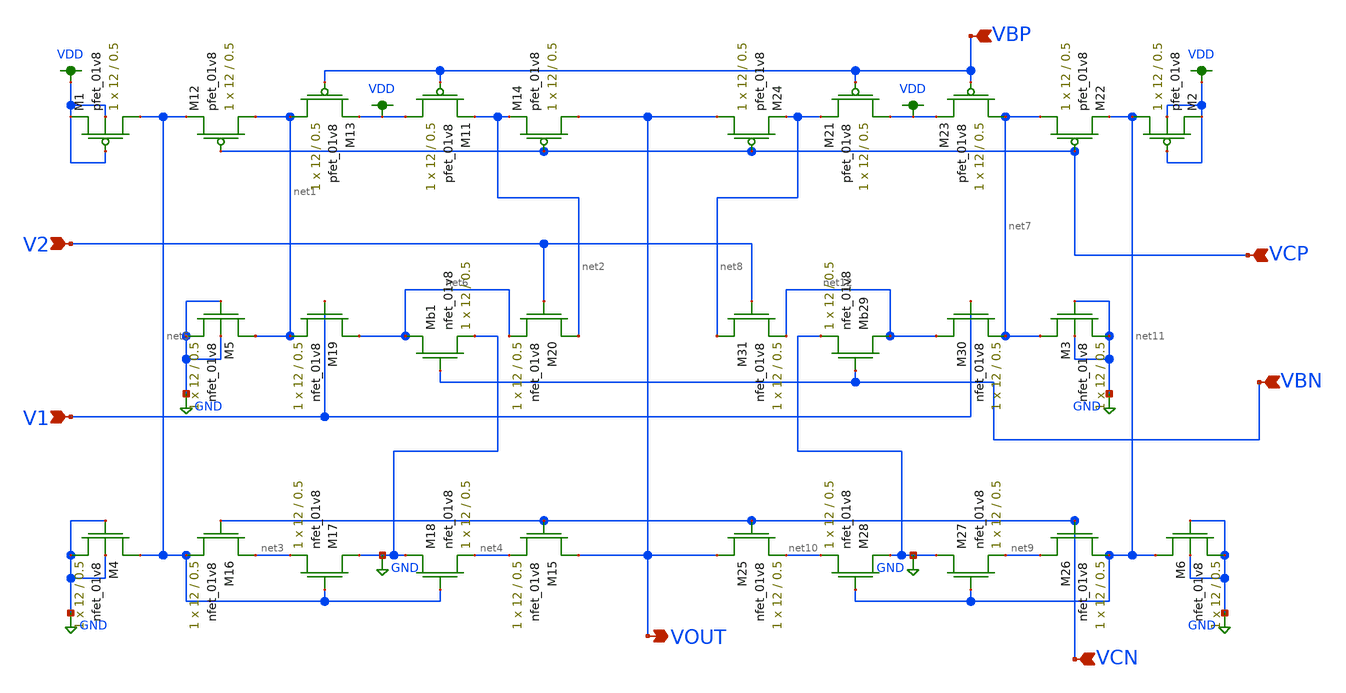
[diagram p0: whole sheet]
** sch_path: MP3/LDS_FCDA.sch
**.subckt LDS_FCDA VBP VCN VCP VOUT VBN V2 V1
*.ipin VBP
*.ipin VCN
*.ipin VCP
*.opin VOUT
*.ipin VBN
*.ipin V2
*.ipin V1
XM11 VDD VBP net2 VDD sky130_fd_pr__pfet_01v8 L=0.5 W=12 nf=1 ad='int((nf+1)/2) * W/nf * 0.29' as='int((nf+2)/2) * W/nf * 0.29'
+ pd='2*int((nf+1)/2) * (W/nf + 0.29)' ps='2*int((nf+2)/2) * (W/nf + 0.29)' nrd='0.29 / W' nrs='0.29 / W'
+ sa=0 sb=0 sd=0 mult=1 m=1
XM12 net1 VCP net5 VDD sky130_fd_pr__pfet_01v8 L=0.5 W=12 nf=1 ad='int((nf+1)/2) * W/nf * 0.29' as='int((nf+2)/2) * W/nf * 0.29'
+ pd='2*int((nf+1)/2) * (W/nf + 0.29)' ps='2*int((nf+2)/2) * (W/nf + 0.29)' nrd='0.29 / W' nrs='0.29 / W'
+ sa=0 sb=0 sd=0 mult=1 m=1
XM13 net1 VBP VDD VDD sky130_fd_pr__pfet_01v8 L=0.5 W=12 nf=1 ad='int((nf+1)/2) * W/nf * 0.29' as='int((nf+2)/2) * W/nf * 0.29'
+ pd='2*int((nf+1)/2) * (W/nf + 0.29)' ps='2*int((nf+2)/2) * (W/nf + 0.29)' nrd='0.29 / W' nrs='0.29 / W'
+ sa=0 sb=0 sd=0 mult=1 m=1
XM14 VOUT VCP net2 VDD sky130_fd_pr__pfet_01v8 L=0.5 W=12 nf=1 ad='int((nf+1)/2) * W/nf * 0.29' as='int((nf+2)/2) * W/nf * 0.29'
+ pd='2*int((nf+1)/2) * (W/nf + 0.29)' ps='2*int((nf+2)/2) * (W/nf + 0.29)' nrd='0.29 / W' nrs='0.29 / W'
+ sa=0 sb=0 sd=0 mult=1 m=1
XM15 VOUT VCN net4 GND sky130_fd_pr__nfet_01v8 L=0.5 W=12 nf=1 ad='int((nf+1)/2) * W/nf * 0.29' as='int((nf+2)/2) * W/nf * 0.29'
+ pd='2*int((nf+1)/2) * (W/nf + 0.29)' ps='2*int((nf+2)/2) * (W/nf + 0.29)' nrd='0.29 / W' nrs='0.29 / W'
+ sa=0 sb=0 sd=0 mult=1 m=1
XM16 net3 VCN net5 GND sky130_fd_pr__nfet_01v8 L=0.5 W=12 nf=1 ad='int((nf+1)/2) * W/nf * 0.29' as='int((nf+2)/2) * W/nf * 0.29'
+ pd='2*int((nf+1)/2) * (W/nf + 0.29)' ps='2*int((nf+2)/2) * (W/nf + 0.29)' nrd='0.29 / W' nrs='0.29 / W'
+ sa=0 sb=0 sd=0 mult=1 m=1
XM17 GND net5 net3 GND sky130_fd_pr__nfet_01v8 L=0.5 W=12 nf=1 ad='int((nf+1)/2) * W/nf * 0.29' as='int((nf+2)/2) * W/nf * 0.29'
+ pd='2*int((nf+1)/2) * (W/nf + 0.29)' ps='2*int((nf+2)/2) * (W/nf + 0.29)' nrd='0.29 / W' nrs='0.29 / W'
+ sa=0 sb=0 sd=0 mult=1 m=1
XM18 GND net5 net4 GND sky130_fd_pr__nfet_01v8 L=0.5 W=12 nf=1 ad='int((nf+1)/2) * W/nf * 0.29' as='int((nf+2)/2) * W/nf * 0.29'
+ pd='2*int((nf+1)/2) * (W/nf + 0.29)' ps='2*int((nf+2)/2) * (W/nf + 0.29)' nrd='0.29 / W' nrs='0.29 / W'
+ sa=0 sb=0 sd=0 mult=1 m=1
XMb1 net6 VBN GND GND sky130_fd_pr__nfet_01v8 L=0.5 W=12 nf=1 ad='int((nf+1)/2) * W/nf * 0.29' as='int((nf+2)/2) * W/nf * 0.29'
+ pd='2*int((nf+1)/2) * (W/nf + 0.29)' ps='2*int((nf+2)/2) * (W/nf + 0.29)' nrd='0.29 / W' nrs='0.29 / W'
+ sa=0 sb=0 sd=0 mult=1 m=1
XM19 net6 V1 net1 GND sky130_fd_pr__nfet_01v8 L=0.5 W=12 nf=1 ad='int((nf+1)/2) * W/nf * 0.29' as='int((nf+2)/2) * W/nf * 0.29'
+ pd='2*int((nf+1)/2) * (W/nf + 0.29)' ps='2*int((nf+2)/2) * (W/nf + 0.29)' nrd='0.29 / W' nrs='0.29 / W'
+ sa=0 sb=0 sd=0 mult=1 m=1
XM20 net2 V2 net6 GND sky130_fd_pr__nfet_01v8 L=0.5 W=12 nf=1 ad='int((nf+1)/2) * W/nf * 0.29' as='int((nf+2)/2) * W/nf * 0.29'
+ pd='2*int((nf+1)/2) * (W/nf + 0.29)' ps='2*int((nf+2)/2) * (W/nf + 0.29)' nrd='0.29 / W' nrs='0.29 / W'
+ sa=0 sb=0 sd=0 mult=1 m=1
XM21 VDD VBP net8 VDD sky130_fd_pr__pfet_01v8 L=0.5 W=12 nf=1 ad='int((nf+1)/2) * W/nf * 0.29' as='int((nf+2)/2) * W/nf * 0.29'
+ pd='2*int((nf+1)/2) * (W/nf + 0.29)' ps='2*int((nf+2)/2) * (W/nf + 0.29)' nrd='0.29 / W' nrs='0.29 / W'
+ sa=0 sb=0 sd=0 mult=1 m=1
XM22 net7 VCP net11 VDD sky130_fd_pr__pfet_01v8 L=0.5 W=12 nf=1 ad='int((nf+1)/2) * W/nf * 0.29' as='int((nf+2)/2) * W/nf * 0.29'
+ pd='2*int((nf+1)/2) * (W/nf + 0.29)' ps='2*int((nf+2)/2) * (W/nf + 0.29)' nrd='0.29 / W' nrs='0.29 / W'
+ sa=0 sb=0 sd=0 mult=1 m=1
XM23 net7 VBP VDD VDD sky130_fd_pr__pfet_01v8 L=0.5 W=12 nf=1 ad='int((nf+1)/2) * W/nf * 0.29' as='int((nf+2)/2) * W/nf * 0.29'
+ pd='2*int((nf+1)/2) * (W/nf + 0.29)' ps='2*int((nf+2)/2) * (W/nf + 0.29)' nrd='0.29 / W' nrs='0.29 / W'
+ sa=0 sb=0 sd=0 mult=1 m=1
XM24 VOUT VCP net8 VDD sky130_fd_pr__pfet_01v8 L=0.5 W=12 nf=1 ad='int((nf+1)/2) * W/nf * 0.29' as='int((nf+2)/2) * W/nf * 0.29'
+ pd='2*int((nf+1)/2) * (W/nf + 0.29)' ps='2*int((nf+2)/2) * (W/nf + 0.29)' nrd='0.29 / W' nrs='0.29 / W'
+ sa=0 sb=0 sd=0 mult=1 m=1
XM25 VOUT VCN net10 GND sky130_fd_pr__nfet_01v8 L=0.5 W=12 nf=1 ad='int((nf+1)/2) * W/nf * 0.29' as='int((nf+2)/2) * W/nf * 0.29'
+ pd='2*int((nf+1)/2) * (W/nf + 0.29)' ps='2*int((nf+2)/2) * (W/nf + 0.29)' nrd='0.29 / W' nrs='0.29 / W'
+ sa=0 sb=0 sd=0 mult=1 m=1
XM26 net9 VCN net11 GND sky130_fd_pr__nfet_01v8 L=0.5 W=12 nf=1 ad='int((nf+1)/2) * W/nf * 0.29' as='int((nf+2)/2) * W/nf * 0.29'
+ pd='2*int((nf+1)/2) * (W/nf + 0.29)' ps='2*int((nf+2)/2) * (W/nf + 0.29)' nrd='0.29 / W' nrs='0.29 / W'
+ sa=0 sb=0 sd=0 mult=1 m=1
XM27 GND net11 net9 GND sky130_fd_pr__nfet_01v8 L=0.5 W=12 nf=1 ad='int((nf+1)/2) * W/nf * 0.29' as='int((nf+2)/2) * W/nf * 0.29'
+ pd='2*int((nf+1)/2) * (W/nf + 0.29)' ps='2*int((nf+2)/2) * (W/nf + 0.29)' nrd='0.29 / W' nrs='0.29 / W'
+ sa=0 sb=0 sd=0 mult=1 m=1
XM28 GND net11 net10 GND sky130_fd_pr__nfet_01v8 L=0.5 W=12 nf=1 ad='int((nf+1)/2) * W/nf * 0.29' as='int((nf+2)/2) * W/nf * 0.29'
+ pd='2*int((nf+1)/2) * (W/nf + 0.29)' ps='2*int((nf+2)/2) * (W/nf + 0.29)' nrd='0.29 / W' nrs='0.29 / W'
+ sa=0 sb=0 sd=0 mult=1 m=1
XMb29 net12 VBN GND GND sky130_fd_pr__nfet_01v8 L=0.5 W=12 nf=1 ad='int((nf+1)/2) * W/nf * 0.29' as='int((nf+2)/2) * W/nf * 0.29'
+ pd='2*int((nf+1)/2) * (W/nf + 0.29)' ps='2*int((nf+2)/2) * (W/nf + 0.29)' nrd='0.29 / W' nrs='0.29 / W'
+ sa=0 sb=0 sd=0 mult=1 m=1
XM30 net12 V1 net7 GND sky130_fd_pr__nfet_01v8 L=0.5 W=12 nf=1 ad='int((nf+1)/2) * W/nf * 0.29' as='int((nf+2)/2) * W/nf * 0.29'
+ pd='2*int((nf+1)/2) * (W/nf + 0.29)' ps='2*int((nf+2)/2) * (W/nf + 0.29)' nrd='0.29 / W' nrs='0.29 / W'
+ sa=0 sb=0 sd=0 mult=1 m=1
XM31 net8 V2 net12 GND sky130_fd_pr__nfet_01v8 L=0.5 W=12 nf=1 ad='int((nf+1)/2) * W/nf * 0.29' as='int((nf+2)/2) * W/nf * 0.29'
+ pd='2*int((nf+1)/2) * (W/nf + 0.29)' ps='2*int((nf+2)/2) * (W/nf + 0.29)' nrd='0.29 / W' nrs='0.29 / W'
+ sa=0 sb=0 sd=0 mult=1 m=1
XM1 net5 VDD VDD VDD sky130_fd_pr__pfet_01v8 L=0.5 W=12 nf=1 ad='int((nf+1)/2) * W/nf * 0.29' as='int((nf+2)/2) * W/nf * 0.29'
+ pd='2*int((nf+1)/2) * (W/nf + 0.29)' ps='2*int((nf+2)/2) * (W/nf + 0.29)' nrd='0.29 / W' nrs='0.29 / W'
+ sa=0 sb=0 sd=0 mult=1 m=1
XM2 net11 VDD VDD VDD sky130_fd_pr__pfet_01v8 L=0.5 W=12 nf=1 ad='int((nf+1)/2) * W/nf * 0.29' as='int((nf+2)/2) * W/nf * 0.29'
+ pd='2*int((nf+1)/2) * (W/nf + 0.29)' ps='2*int((nf+2)/2) * (W/nf + 0.29)' nrd='0.29 / W' nrs='0.29 / W'
+ sa=0 sb=0 sd=0 mult=1 m=1
XM4 net5 GND GND GND sky130_fd_pr__nfet_01v8 L=0.5 W=12 nf=1 ad='int((nf+1)/2) * W/nf * 0.29' as='int((nf+2)/2) * W/nf * 0.29'
+ pd='2*int((nf+1)/2) * (W/nf + 0.29)' ps='2*int((nf+2)/2) * (W/nf + 0.29)' nrd='0.29 / W' nrs='0.29 / W'
+ sa=0 sb=0 sd=0 mult=1 m=1
XM3 net7 GND GND GND sky130_fd_pr__nfet_01v8 L=0.5 W=12 nf=1 ad='int((nf+1)/2) * W/nf * 0.29' as='int((nf+2)/2) * W/nf * 0.29'
+ pd='2*int((nf+1)/2) * (W/nf + 0.29)' ps='2*int((nf+2)/2) * (W/nf + 0.29)' nrd='0.29 / W' nrs='0.29 / W'
+ sa=0 sb=0 sd=0 mult=1 m=1
XM5 net1 GND GND GND sky130_fd_pr__nfet_01v8 L=0.5 W=12 nf=1 ad='int((nf+1)/2) * W/nf * 0.29' as='int((nf+2)/2) * W/nf * 0.29'
+ pd='2*int((nf+1)/2) * (W/nf + 0.29)' ps='2*int((nf+2)/2) * (W/nf + 0.29)' nrd='0.29 / W' nrs='0.29 / W'
+ sa=0 sb=0 sd=0 mult=1 m=1
XM6 net11 GND GND GND sky130_fd_pr__nfet_01v8 L=0.5 W=12 nf=1 ad='int((nf+1)/2) * W/nf * 0.29' as='int((nf+2)/2) * W/nf * 0.29'
+ pd='2*int((nf+1)/2) * (W/nf + 0.29)' ps='2*int((nf+2)/2) * (W/nf + 0.29)' nrd='0.29 / W' nrs='0.29 / W'
+ sa=0 sb=0 sd=0 mult=1 m=1
**.ends
.GLOBAL VDD
.GLOBAL GND
.end
